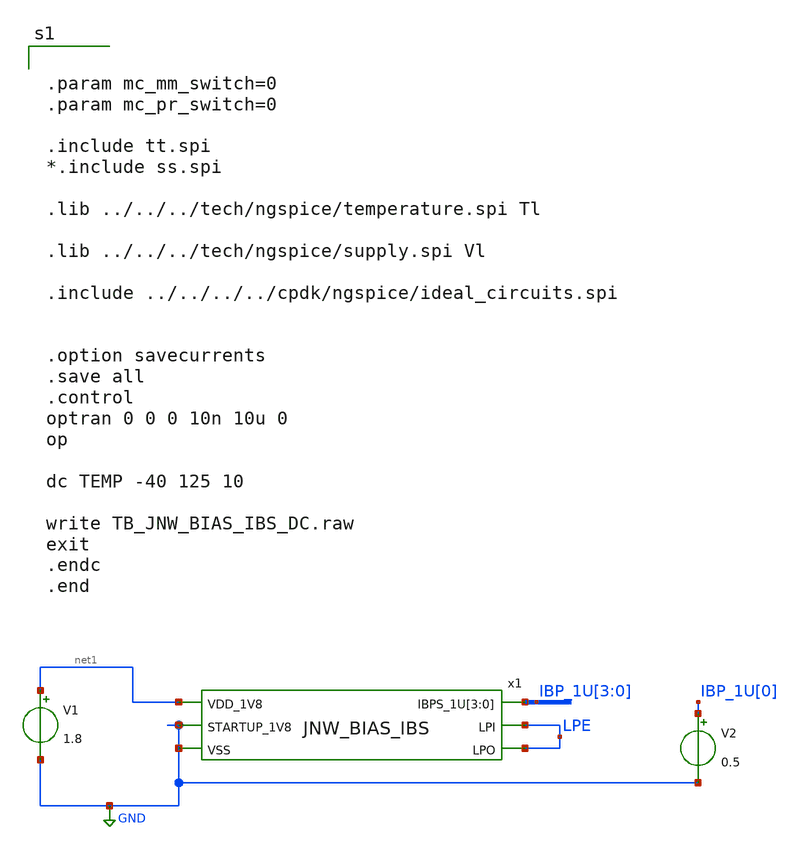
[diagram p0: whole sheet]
** sch_path: design/JNW_BIAS_SKY130A/TB_JNW_BIAS_IBPS_DC.sch
**.subckt TB_JNW_BIAS_IBPS_DC
x1 net1 IBP_1U[3] IBP_1U[2] IBP_1U[1] IBP_1U[0] LPE LPE GND GND JNW_BIAS_IBS
V1 net1 GND 1.8
V2 IBP_1U[0] GND 0.5
**** begin user architecture code


.param mc_mm_switch=0
.param mc_pr_switch=0

.include tt.spi
*.include ss.spi

.lib ../../../tech/ngspice/temperature.spi Tl

.lib ../../../tech/ngspice/supply.spi Vl

.include ../../../../cpdk/ngspice/ideal_circuits.spi


.option savecurrents
.save all
.control
optran 0 0 0 10n 10u 0
op

dc TEMP -40 125 10

write TB_JNW_BIAS_IBS_DC.raw
exit
.endc
.end



**** end user architecture code
**.ends
.GLOBAL GND
.end
